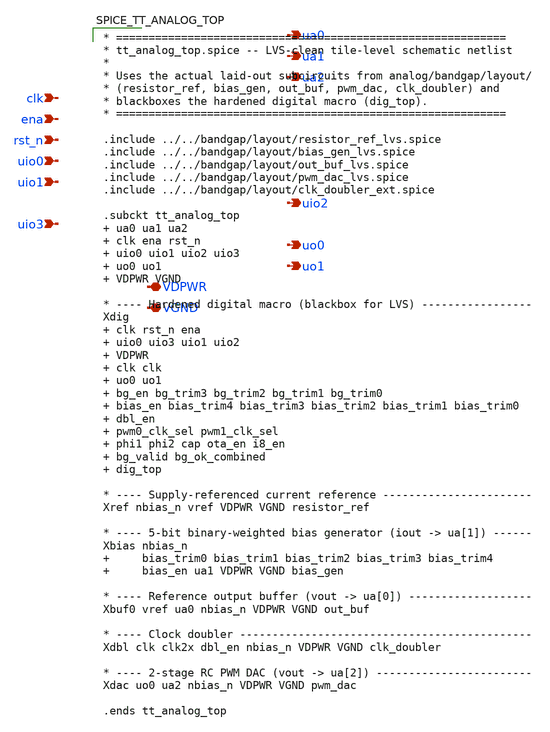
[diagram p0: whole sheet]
** sch_path: bvm_analog_tapeout/analog/tt_analog_top/xschem/tt_analog_top.sch
**.subckt tt_analog_top ua0 ua1 ua2 clk ena rst_n uio0 uio1 uio2 uio3 uo0 uo1 VDPWR VGND
*.opin ua0
*.opin ua1
*.opin ua2
*.ipin clk
*.ipin ena
*.ipin rst_n
*.ipin uio0
*.ipin uio1
*.opin uio2
*.ipin uio3
*.opin uo0
*.opin uo1
*.iopin VDPWR
*.iopin VGND
**** begin user architecture code

* ============================================================
* tt_analog_top.spice -- LVS-clean tile-level schematic netlist
*
* Uses the actual laid-out subcircuits from analog/bandgap/layout/
* (resistor_ref, bias_gen, out_buf, pwm_dac, clk_doubler) and
* blackboxes the hardened digital macro (dig_top).
* ============================================================

.include ../../bandgap/layout/resistor_ref_lvs.spice
.include ../../bandgap/layout/bias_gen_lvs.spice
.include ../../bandgap/layout/out_buf_lvs.spice
.include ../../bandgap/layout/pwm_dac_lvs.spice
.include ../../bandgap/layout/clk_doubler_ext.spice

.subckt tt_analog_top  ua0 ua1 ua2  clk ena rst_n  uio0 uio1 uio2 uio3  uo0 uo1  VDPWR VGND

* ---- Hardened digital macro (blackbox for LVS) -----------------
Xdig  clk rst_n ena  uio0 uio3 uio1 uio2  VDPWR  clk clk  uo0 uo1  bg_en bg_trim3 bg_trim2 bg_trim1
+ bg_trim0  bias_en bias_trim4 bias_trim3 bias_trim2 bias_trim1 bias_trim0  dbl_en  pwm0_clk_sel pwm1_clk_sel
+  phi1 phi2 cap ota_en i8_en  bg_valid bg_ok_combined  dig_top

* ---- Supply-referenced current reference -----------------------
Xref nbias_n vref VDPWR VGND resistor_ref

* ---- 5-bit binary-weighted bias generator (iout -> ua[1]) ------
Xbias nbias_n      bias_trim0 bias_trim1 bias_trim2 bias_trim3 bias_trim4      bias_en ua1 VDPWR
+ VGND bias_gen

* ---- Reference output buffer (vout -> ua[0]) -------------------
Xbuf0 vref ua0 nbias_n VDPWR VGND out_buf

* ---- Clock doubler ---------------------------------------------
Xdbl clk clk2x dbl_en nbias_n VDPWR VGND clk_doubler

* ---- 2-stage RC PWM DAC (vout -> ua[2]) ------------------------
Xdac uo0 ua2 nbias_n VDPWR VGND pwm_dac

.ends tt_analog_top


**** end user architecture code
**.ends
.end
